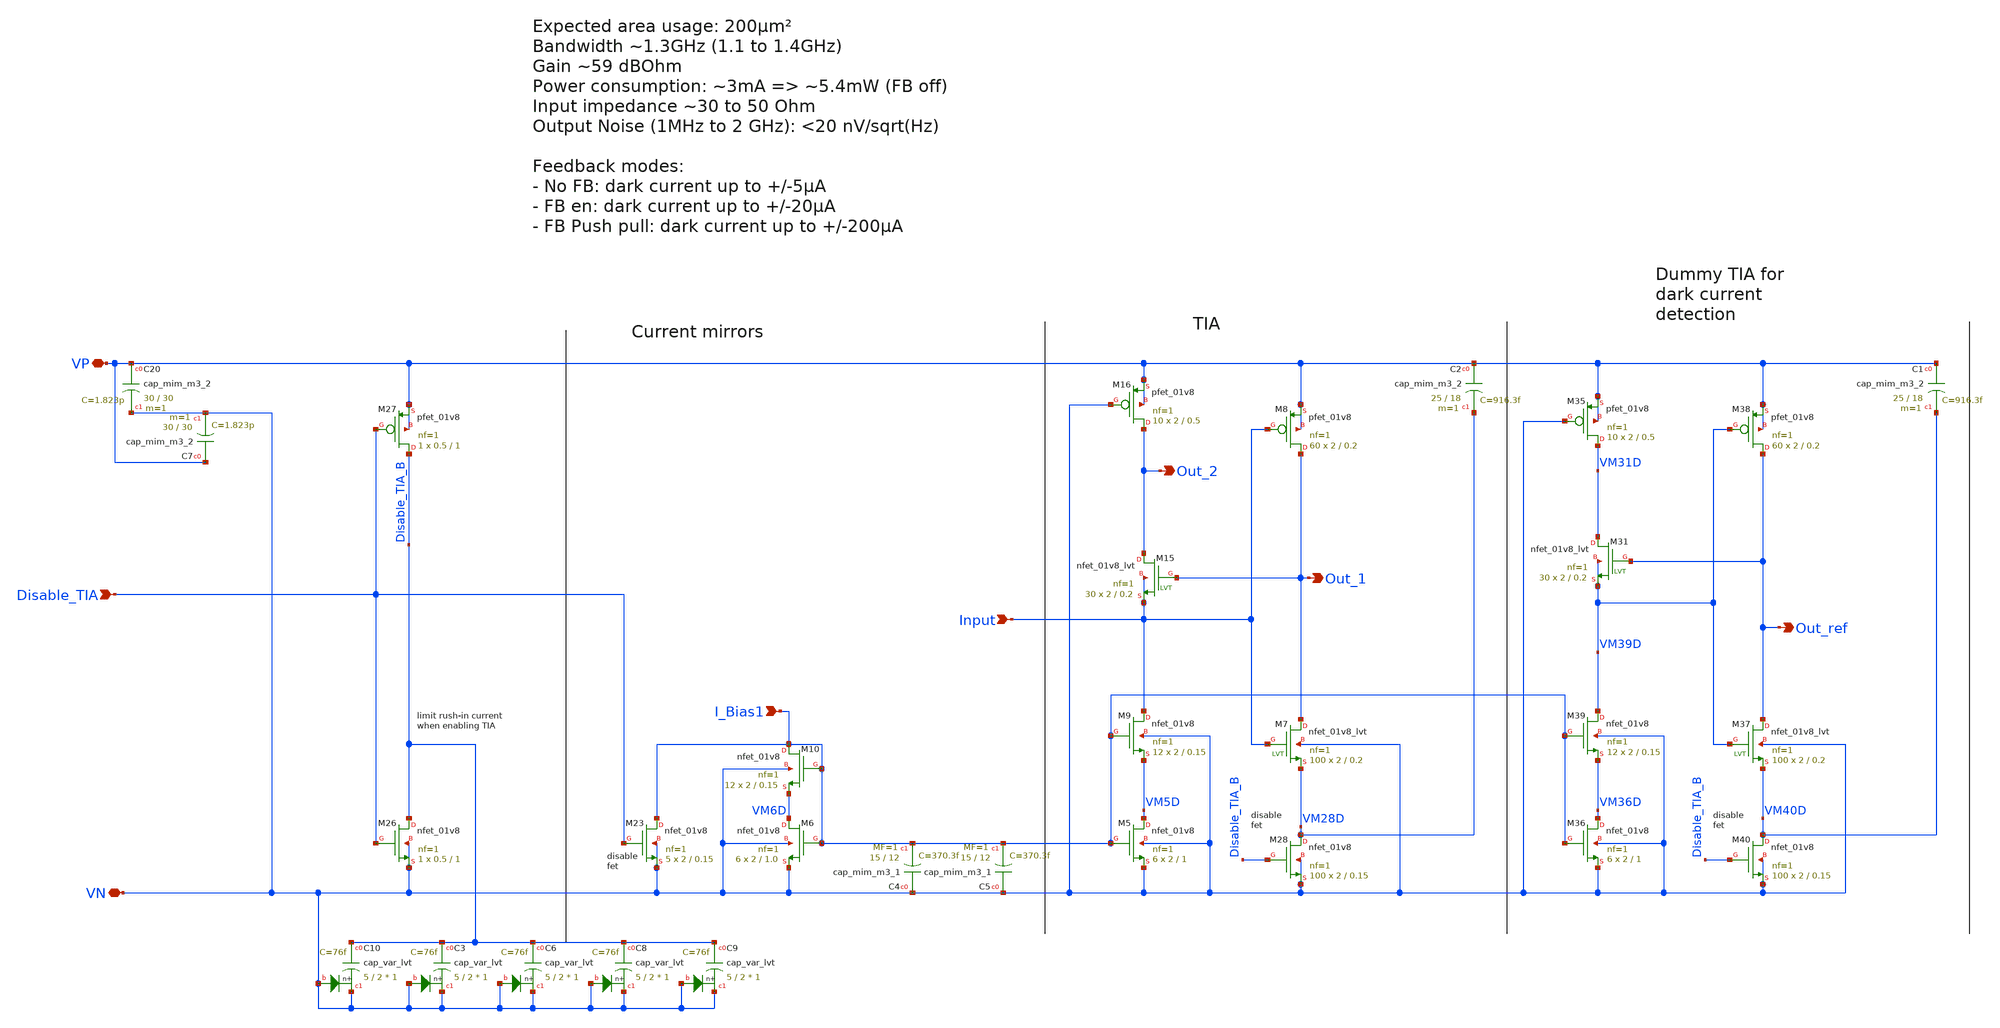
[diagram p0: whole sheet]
** sch_path: xschem/tia/tia_rgc_core.sch
**.subckt tia_rgc_core VN VP Out_2 I_Bias1 Input Disable_TIA Out_1 Out_ref
*.iopin VN
*.iopin VP
*.opin Out_2
*.ipin I_Bias1
*.ipin Input
*.ipin Disable_TIA
*.opin Out_1
*.opin Out_ref
XM5 VM5D I_Bias1 VN VN sky130_fd_pr__nfet_01v8 L=1 W=2 nf=1 ad='int((nf+1)/2) * W/nf * 0.29' as='int((nf+2)/2) * W/nf * 0.29'
+ pd='2*int((nf+1)/2) * (W/nf + 0.29)' ps='2*int((nf+2)/2) * (W/nf + 0.29)' nrd='0.29 / W' nrs='0.29 / W'
+ sa=0 sb=0 sd=0 mult=6 m=6
XM6 VM6D I_Bias1 VN VN sky130_fd_pr__nfet_01v8 L=1.0 W=2 nf=1 ad='int((nf+1)/2) * W/nf * 0.29' as='int((nf+2)/2) * W/nf * 0.29'
+ pd='2*int((nf+1)/2) * (W/nf + 0.29)' ps='2*int((nf+2)/2) * (W/nf + 0.29)' nrd='0.29 / W' nrs='0.29 / W'
+ sa=0 sb=0 sd=0 mult=6 m=6
XM7 Out_1 Input VM28D VN sky130_fd_pr__nfet_01v8_lvt L=0.2 W=2 nf=1 ad='int((nf+1)/2) * W/nf * 0.29'
+ as='int((nf+2)/2) * W/nf * 0.29' pd='2*int((nf+1)/2) * (W/nf + 0.29)' ps='2*int((nf+2)/2) * (W/nf + 0.29)'
+ nrd='0.29 / W' nrs='0.29 / W' sa=0 sb=0 sd=0 mult=100 m=100
XM8 Out_1 Input VP VP sky130_fd_pr__pfet_01v8 L=0.2 W=2 nf=1 ad='int((nf+1)/2) * W/nf * 0.29' as='int((nf+2)/2) * W/nf * 0.29'
+ pd='2*int((nf+1)/2) * (W/nf + 0.29)' ps='2*int((nf+2)/2) * (W/nf + 0.29)' nrd='0.29 / W' nrs='0.29 / W'
+ sa=0 sb=0 sd=0 mult=60 m=60
XM9 Input I_Bias1 VM5D VN sky130_fd_pr__nfet_01v8 L=0.15 W=2 nf=1 ad='int((nf+1)/2) * W/nf * 0.29' as='int((nf+2)/2) * W/nf * 0.29'
+ pd='2*int((nf+1)/2) * (W/nf + 0.29)' ps='2*int((nf+2)/2) * (W/nf + 0.29)' nrd='0.29 / W' nrs='0.29 / W'
+ sa=0 sb=0 sd=0 mult=12 m=12
XM10 I_Bias1 I_Bias1 VM6D VN sky130_fd_pr__nfet_01v8 L=0.15 W=2 nf=1 ad='int((nf+1)/2) * W/nf * 0.29'
+ as='int((nf+2)/2) * W/nf * 0.29' pd='2*int((nf+1)/2) * (W/nf + 0.29)' ps='2*int((nf+2)/2) * (W/nf + 0.29)'
+ nrd='0.29 / W' nrs='0.29 / W' sa=0 sb=0 sd=0 mult=12 m=12
XM23 I_Bias1 Disable_TIA VN VN sky130_fd_pr__nfet_01v8 L=0.15 W=2 nf=1 ad='int((nf+1)/2) * W/nf * 0.29'
+ as='int((nf+2)/2) * W/nf * 0.29' pd='2*int((nf+1)/2) * (W/nf + 0.29)' ps='2*int((nf+2)/2) * (W/nf + 0.29)'
+ nrd='0.29 / W' nrs='0.29 / W' sa=0 sb=0 sd=0 mult=5 m=5
XM26 Disable_TIA_B Disable_TIA VN VN sky130_fd_pr__nfet_01v8 L=1 W=0.5 nf=1 ad='int((nf+1)/2) * W/nf * 0.29'
+ as='int((nf+2)/2) * W/nf * 0.29' pd='2*int((nf+1)/2) * (W/nf + 0.29)' ps='2*int((nf+2)/2) * (W/nf + 0.29)'
+ nrd='0.29 / W' nrs='0.29 / W' sa=0 sb=0 sd=0 mult=1 m=1
XM27 Disable_TIA_B Disable_TIA VP VP sky130_fd_pr__pfet_01v8 L=1 W=0.5 nf=1 ad='int((nf+1)/2) * W/nf * 0.29'
+ as='int((nf+2)/2) * W/nf * 0.29' pd='2*int((nf+1)/2) * (W/nf + 0.29)' ps='2*int((nf+2)/2) * (W/nf + 0.29)'
+ nrd='0.29 / W' nrs='0.29 / W' sa=0 sb=0 sd=0 mult=1 m=1
XM28 VM28D Disable_TIA_B VN VN sky130_fd_pr__nfet_01v8 L=0.15 W=2 nf=1 ad='int((nf+1)/2) * W/nf * 0.29'
+ as='int((nf+2)/2) * W/nf * 0.29' pd='2*int((nf+1)/2) * (W/nf + 0.29)' ps='2*int((nf+2)/2) * (W/nf + 0.29)'
+ nrd='0.29 / W' nrs='0.29 / W' sa=0 sb=0 sd=0 mult=100 m=100
XM36 VM36D I_Bias1 VN VN sky130_fd_pr__nfet_01v8 L=1 W=2 nf=1 ad='int((nf+1)/2) * W/nf * 0.29' as='int((nf+2)/2) * W/nf * 0.29'
+ pd='2*int((nf+1)/2) * (W/nf + 0.29)' ps='2*int((nf+2)/2) * (W/nf + 0.29)' nrd='0.29 / W' nrs='0.29 / W'
+ sa=0 sb=0 sd=0 mult=6 m=6
XM37 Out_ref VM39D VM40D VN sky130_fd_pr__nfet_01v8_lvt L=0.2 W=2 nf=1 ad='int((nf+1)/2) * W/nf * 0.29'
+ as='int((nf+2)/2) * W/nf * 0.29' pd='2*int((nf+1)/2) * (W/nf + 0.29)' ps='2*int((nf+2)/2) * (W/nf + 0.29)'
+ nrd='0.29 / W' nrs='0.29 / W' sa=0 sb=0 sd=0 mult=100 m=100
XM38 Out_ref VM39D VP VP sky130_fd_pr__pfet_01v8 L=0.2 W=2 nf=1 ad='int((nf+1)/2) * W/nf * 0.29' as='int((nf+2)/2) * W/nf * 0.29'
+ pd='2*int((nf+1)/2) * (W/nf + 0.29)' ps='2*int((nf+2)/2) * (W/nf + 0.29)' nrd='0.29 / W' nrs='0.29 / W'
+ sa=0 sb=0 sd=0 mult=60 m=60
XM39 VM39D I_Bias1 VM36D VN sky130_fd_pr__nfet_01v8 L=0.15 W=2 nf=1 ad='int((nf+1)/2) * W/nf * 0.29'
+ as='int((nf+2)/2) * W/nf * 0.29' pd='2*int((nf+1)/2) * (W/nf + 0.29)' ps='2*int((nf+2)/2) * (W/nf + 0.29)'
+ nrd='0.29 / W' nrs='0.29 / W' sa=0 sb=0 sd=0 mult=12 m=12
XM40 VM40D Disable_TIA_B VN VN sky130_fd_pr__nfet_01v8 L=0.15 W=2 nf=1 ad='int((nf+1)/2) * W/nf * 0.29'
+ as='int((nf+2)/2) * W/nf * 0.29' pd='2*int((nf+1)/2) * (W/nf + 0.29)' ps='2*int((nf+2)/2) * (W/nf + 0.29)'
+ nrd='0.29 / W' nrs='0.29 / W' sa=0 sb=0 sd=0 mult=100 m=100
XC20 VP VN sky130_fd_pr__cap_mim_m3_2 W=30 L=30 MF=1 m=1
XM16 Out_2 VN VP VP sky130_fd_pr__pfet_01v8 L=0.5 W=2 nf=1 ad='int((nf+1)/2) * W/nf * 0.29' as='int((nf+2)/2) * W/nf * 0.29'
+ pd='2*int((nf+1)/2) * (W/nf + 0.29)' ps='2*int((nf+2)/2) * (W/nf + 0.29)' nrd='0.29 / W' nrs='0.29 / W'
+ sa=0 sb=0 sd=0 mult=10 m=10
XM15 Out_2 Out_1 Input Input sky130_fd_pr__nfet_01v8_lvt L=0.2 W=2 nf=1 ad='int((nf+1)/2) * W/nf * 0.29'
+ as='int((nf+2)/2) * W/nf * 0.29' pd='2*int((nf+1)/2) * (W/nf + 0.29)' ps='2*int((nf+2)/2) * (W/nf + 0.29)'
+ nrd='0.29 / W' nrs='0.29 / W' sa=0 sb=0 sd=0 mult=30 m=30
XM31 VM31D Out_ref VM39D VM39D sky130_fd_pr__nfet_01v8_lvt L=0.2 W=2 nf=1 ad='int((nf+1)/2) * W/nf * 0.29'
+ as='int((nf+2)/2) * W/nf * 0.29' pd='2*int((nf+1)/2) * (W/nf + 0.29)' ps='2*int((nf+2)/2) * (W/nf + 0.29)'
+ nrd='0.29 / W' nrs='0.29 / W' sa=0 sb=0 sd=0 mult=30 m=30
XM35 VM31D VN VP VP sky130_fd_pr__pfet_01v8 L=0.5 W=2 nf=1 ad='int((nf+1)/2) * W/nf * 0.29' as='int((nf+2)/2) * W/nf * 0.29'
+ pd='2*int((nf+1)/2) * (W/nf + 0.29)' ps='2*int((nf+2)/2) * (W/nf + 0.29)' nrd='0.29 / W' nrs='0.29 / W'
+ sa=0 sb=0 sd=0 mult=10 m=10
XC7 VP VN sky130_fd_pr__cap_mim_m3_2 W=30 L=30 MF=1 m=1
XC2 VP VM28D sky130_fd_pr__cap_mim_m3_2 W=25 L=18 MF=1 m=1
XC5 VN I_Bias1 sky130_fd_pr__cap_mim_m3_1 W=15 L=12 MF=1 m=1
XC4 VN I_Bias1 sky130_fd_pr__cap_mim_m3_1 W=15 L=12 MF=1 m=1
XC1 VP VM40D sky130_fd_pr__cap_mim_m3_2 W=25 L=18 MF=1 m=1
XC10 Disable_TIA_B VN VN sky130_fd_pr__cap_var_lvt W=5 L=2 VM=1 m=1
XC3 Disable_TIA_B VN VN sky130_fd_pr__cap_var_lvt W=5 L=2 VM=1 m=1
XC6 Disable_TIA_B VN VN sky130_fd_pr__cap_var_lvt W=5 L=2 VM=1 m=1
XC8 Disable_TIA_B VN VN sky130_fd_pr__cap_var_lvt W=5 L=2 VM=1 m=1
XC9 Disable_TIA_B VN VN sky130_fd_pr__cap_var_lvt W=5 L=2 VM=1 m=1
**.ends
.end
